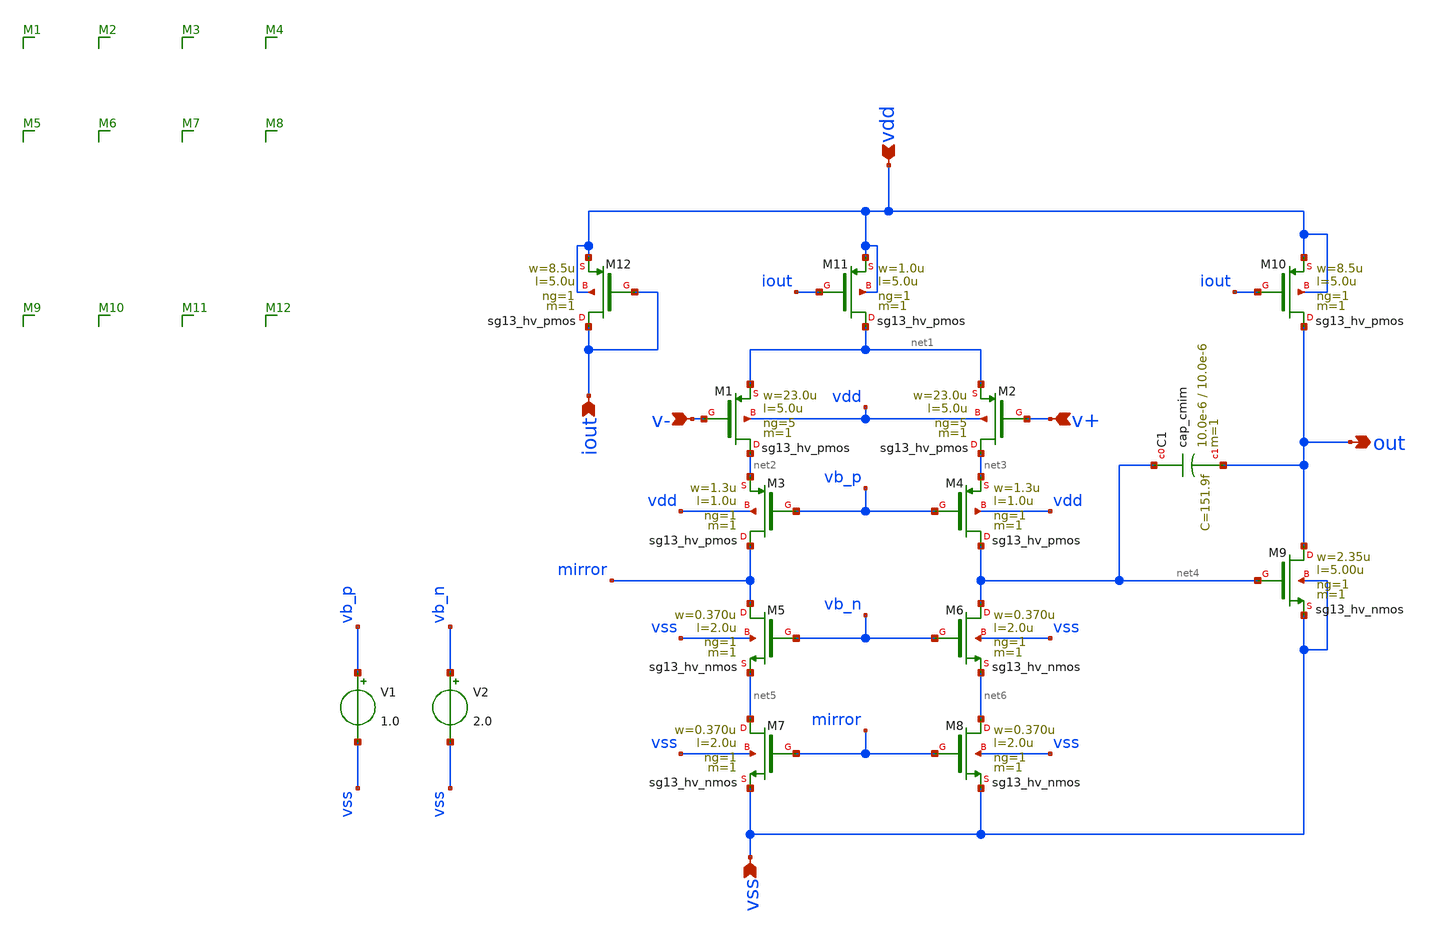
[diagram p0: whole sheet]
** sch_path: schematic/two_stage.sch
**.subckt two_stage out iout v- v+ vdd vss
*.opin out
*.ipin iout
*.ipin v-
*.ipin v+
*.ipin vdd
*.ipin vss
XM1 net2 v- net1 vdd sg13_hv_pmos w=23.0u l=5.0u ng=5 m=1 mm_ok=1
XM2 net3 v+ net1 vdd sg13_hv_pmos w=23.0u l=5.0u ng=5 m=1 mm_ok=1
XM5 mirror vb_n net5 vss sg13_hv_nmos w=0.370u l=2.0u ng=1 m=1 mm_ok=1
XM11 net1 iout vdd vdd sg13_hv_pmos w=1.0u l=5.0u ng=1 m=1 mm_ok=1
XM12 iout iout vdd vdd sg13_hv_pmos w=8.5u l=5.0u ng=1 m=1 mm_ok=1
XM3 mirror vb_p net2 vdd sg13_hv_pmos w=1.3u l=1.0u ng=1 m=1 mm_ok=1
XM4 net4 vb_p net3 vdd sg13_hv_pmos w=1.3u l=1.0u ng=1 m=1 mm_ok=1
XM6 net4 vb_n net6 vss sg13_hv_nmos w=0.370u l=2.0u ng=1 m=1 mm_ok=1
XM7 net5 mirror vss vss sg13_hv_nmos w=0.370u l=2.0u ng=1 m=1 mm_ok=1
XM8 net6 mirror vss vss sg13_hv_nmos w=0.370u l=2.0u ng=1 m=1 mm_ok=1
XM9 out net4 vss vss sg13_hv_nmos w=2.35u l=5.00u ng=1 m=1 mm_ok=1
XC1 net4 out cap_cmim w=10.0e-6 l=10.0e-6 m=1 mm_ok=1
XM10 out iout vdd vdd sg13_hv_pmos w=8.5u l=5.0u ng=1 m=1 mm_ok=1
V1 vb_p vss 1.0
V2 vb_n vss 2.0
**.ends
.end
